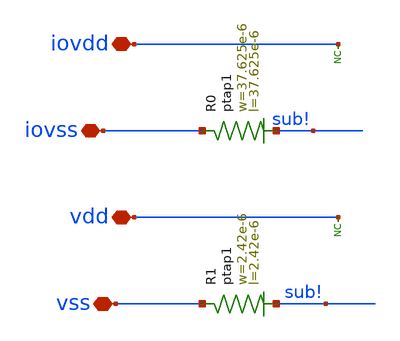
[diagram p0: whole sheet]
** sch_path: ihp-sg13g2/libs.ref/sg13g2_io/sch/xschem/sg13g2_Filler4000.sch
**.subckt sg13g2_Filler4000 iovdd iovss vss vdd
*.iopin iovdd
*.iopin iovss
*.iopin vss
*.iopin vdd
* noconn iovdd
* noconn vdd
XR0 iovss sub! ptap1 R=625.7m w=37.625e-6 l=37.625e-6
XR1 vss sub! ptap1 R=63.08 w=2.42e-6 l=2.42e-6
**.ends
.end
